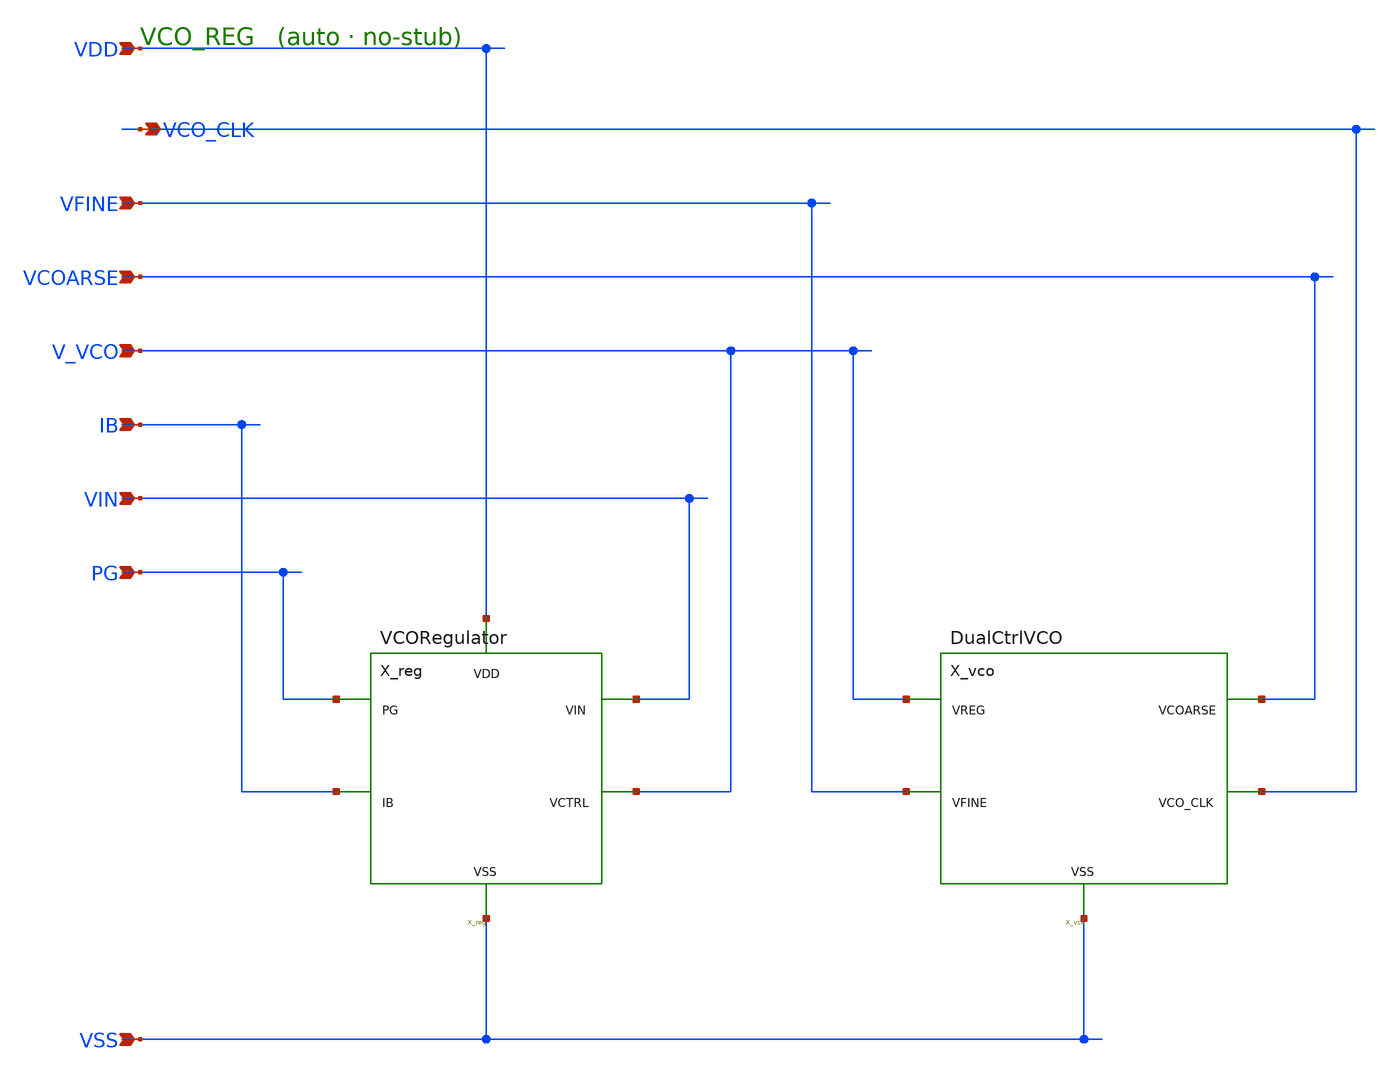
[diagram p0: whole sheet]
** sch_path: schematics/VCO_REG.sch
**.subckt VCO_REG VDD VSS V_VCO PG VIN IB VCOARSE VFINE VCO_CLK
*.ipin VDD
*.ipin VSS
*.ipin V_VCO
*.ipin PG
*.ipin VIN
*.ipin IB
*.ipin VCOARSE
*.ipin VFINE
*.opin VCO_CLK
X_reg VSS PG VIN IB VDD V_VCO VCORegulator
X_vco VSS V_VCO VCOARSE VFINE VCO_CLK DualCtrlVCO
**.ends
.end
